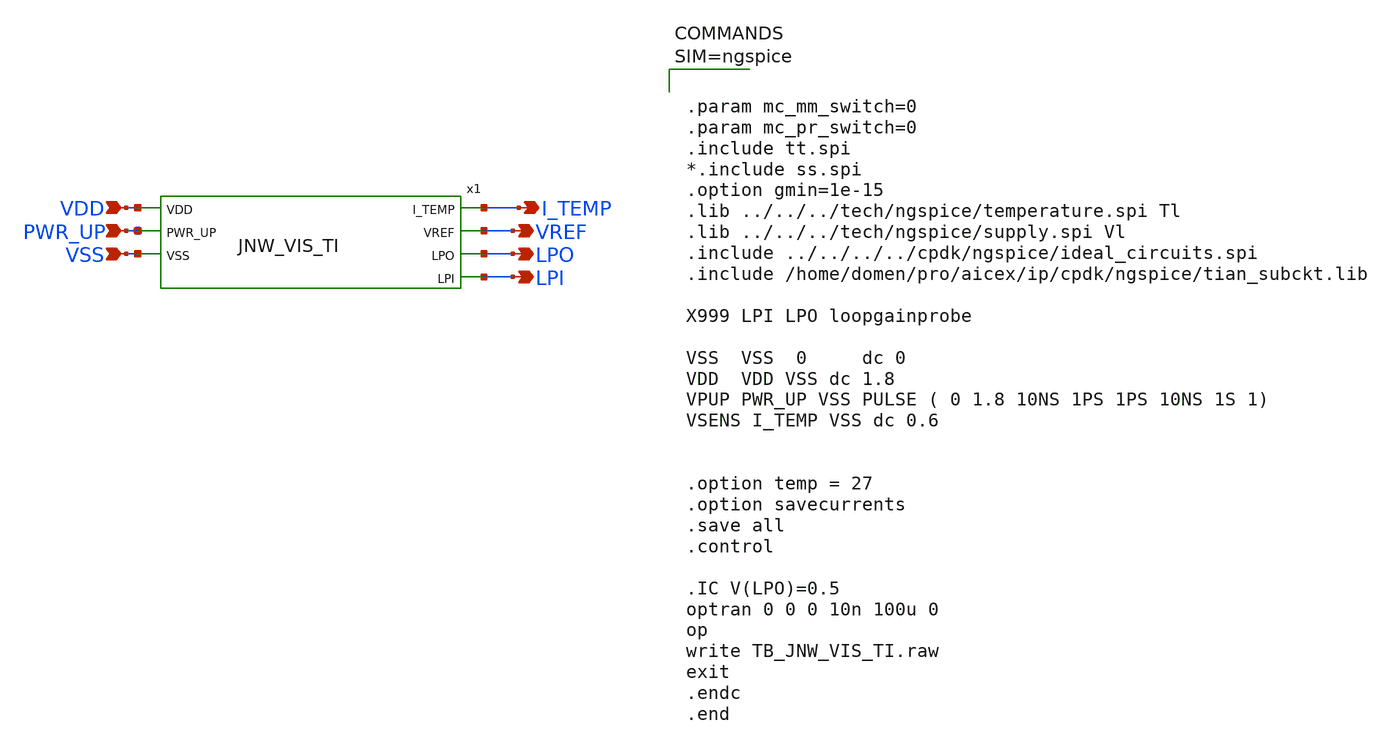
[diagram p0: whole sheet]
** sch_path: design/JNW_GR02_SKY130A/TB_JNW_VIS_TI.sch
**.subckt TB_JNW_VIS_TI VDD VSS VREF I_TEMP PWR_UP LPI LPO
*.ipin VDD
*.ipin VSS
*.opin VREF
*.opin I_TEMP
*.ipin PWR_UP
*.opin LPI
*.opin LPO
x1 I_TEMP VDD VREF LPO LPI PWR_UP VSS JNW_VIS_TI
**** begin user architecture code



.param mc_mm_switch=0
.param mc_pr_switch=0
.include tt.spi
*.include ss.spi
.option gmin=1e-15
.lib ../../../tech/ngspice/temperature.spi Tl
.lib ../../../tech/ngspice/supply.spi Vl
.include ../../../../cpdk/ngspice/ideal_circuits.spi
.include /home/domen/pro/aicex/ip/cpdk/ngspice/tian_subckt.lib

X999 LPI LPO loopgainprobe

VSS  VSS  0     dc 0
VDD  VDD VSS dc 1.8
VPUP PWR_UP VSS PULSE ( 0 1.8 10NS 1PS 1PS 10NS 1S 1)
VSENS I_TEMP VSS dc 0.6


.option temp = 27
.option savecurrents
.save all
.control

.IC V(LPO)=0.5
optran 0 0 0 10n 100u 0
op
write TB_JNW_VIS_TI.raw
exit
.endc
.end




**** end user architecture code
**.ends
.end
